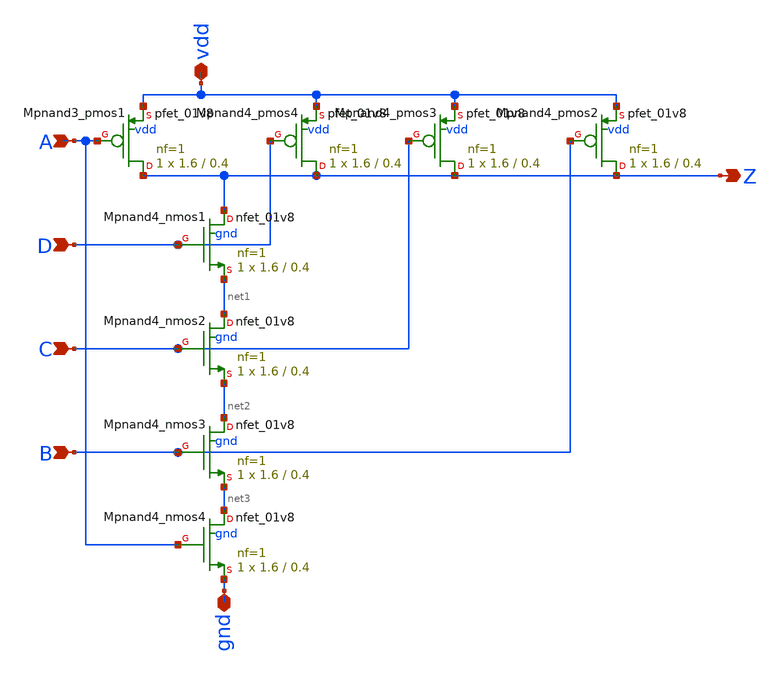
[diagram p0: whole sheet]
** sch_path: sram_4_16_scn4m/pnand4.sch
**.subckt pnand4 D C A B Z vdd gnd
*.ipin D
*.ipin C
*.ipin A
*.ipin B
*.opin Z
*.iopin vdd
*.iopin gnd
XMpnand4_nmos1 Z D net1 gnd sky130_fd_pr__nfet_01v8 L=0.4 W=1.6 nf=1 ad='int((nf+1)/2) * W/nf * 0.29'
+ as='int((nf+2)/2) * W/nf * 0.29' pd='2*int((nf+1)/2) * (W/nf + 0.29)' ps='2*int((nf+2)/2) * (W/nf + 0.29)'
+ nrd='0.29 / W' nrs='0.29 / W' sa=0 sb=0 sd=0 mult=1 m=1
XMpnand3_pmos1 Z A vdd vdd sky130_fd_pr__pfet_01v8 L=0.4 W=1.6 nf=1 ad='int((nf+1)/2) * W/nf * 0.29'
+ as='int((nf+2)/2) * W/nf * 0.29' pd='2*int((nf+1)/2) * (W/nf + 0.29)' ps='2*int((nf+2)/2) * (W/nf + 0.29)'
+ nrd='0.29 / W' nrs='0.29 / W' sa=0 sb=0 sd=0 mult=1 m=1
XMpnand4_pmos4 Z D vdd vdd sky130_fd_pr__pfet_01v8 L=0.4 W=1.6 nf=1 ad='int((nf+1)/2) * W/nf * 0.29'
+ as='int((nf+2)/2) * W/nf * 0.29' pd='2*int((nf+1)/2) * (W/nf + 0.29)' ps='2*int((nf+2)/2) * (W/nf + 0.29)'
+ nrd='0.29 / W' nrs='0.29 / W' sa=0 sb=0 sd=0 mult=1 m=1
XMpnand4_nmos2 net1 C net2 gnd sky130_fd_pr__nfet_01v8 L=0.4 W=1.6 nf=1 ad='int((nf+1)/2) * W/nf * 0.29'
+ as='int((nf+2)/2) * W/nf * 0.29' pd='2*int((nf+1)/2) * (W/nf + 0.29)' ps='2*int((nf+2)/2) * (W/nf + 0.29)'
+ nrd='0.29 / W' nrs='0.29 / W' sa=0 sb=0 sd=0 mult=1 m=1
XMpnand4_pmos3 Z C vdd vdd sky130_fd_pr__pfet_01v8 L=0.4 W=1.6 nf=1 ad='int((nf+1)/2) * W/nf * 0.29'
+ as='int((nf+2)/2) * W/nf * 0.29' pd='2*int((nf+1)/2) * (W/nf + 0.29)' ps='2*int((nf+2)/2) * (W/nf + 0.29)'
+ nrd='0.29 / W' nrs='0.29 / W' sa=0 sb=0 sd=0 mult=1 m=1
XMpnand4_nmos3 net2 B net3 gnd sky130_fd_pr__nfet_01v8 L=0.4 W=1.6 nf=1 ad='int((nf+1)/2) * W/nf * 0.29'
+ as='int((nf+2)/2) * W/nf * 0.29' pd='2*int((nf+1)/2) * (W/nf + 0.29)' ps='2*int((nf+2)/2) * (W/nf + 0.29)'
+ nrd='0.29 / W' nrs='0.29 / W' sa=0 sb=0 sd=0 mult=1 m=1
XMpnand4_pmos2 Z B vdd vdd sky130_fd_pr__pfet_01v8 L=0.4 W=1.6 nf=1 ad='int((nf+1)/2) * W/nf * 0.29'
+ as='int((nf+2)/2) * W/nf * 0.29' pd='2*int((nf+1)/2) * (W/nf + 0.29)' ps='2*int((nf+2)/2) * (W/nf + 0.29)'
+ nrd='0.29 / W' nrs='0.29 / W' sa=0 sb=0 sd=0 mult=1 m=1
XMpnand4_nmos4 net3 A gnd gnd sky130_fd_pr__nfet_01v8 L=0.4 W=1.6 nf=1 ad='int((nf+1)/2) * W/nf * 0.29'
+ as='int((nf+2)/2) * W/nf * 0.29' pd='2*int((nf+1)/2) * (W/nf + 0.29)' ps='2*int((nf+2)/2) * (W/nf + 0.29)'
+ nrd='0.29 / W' nrs='0.29 / W' sa=0 sb=0 sd=0 mult=1 m=1
**.ends
.end
